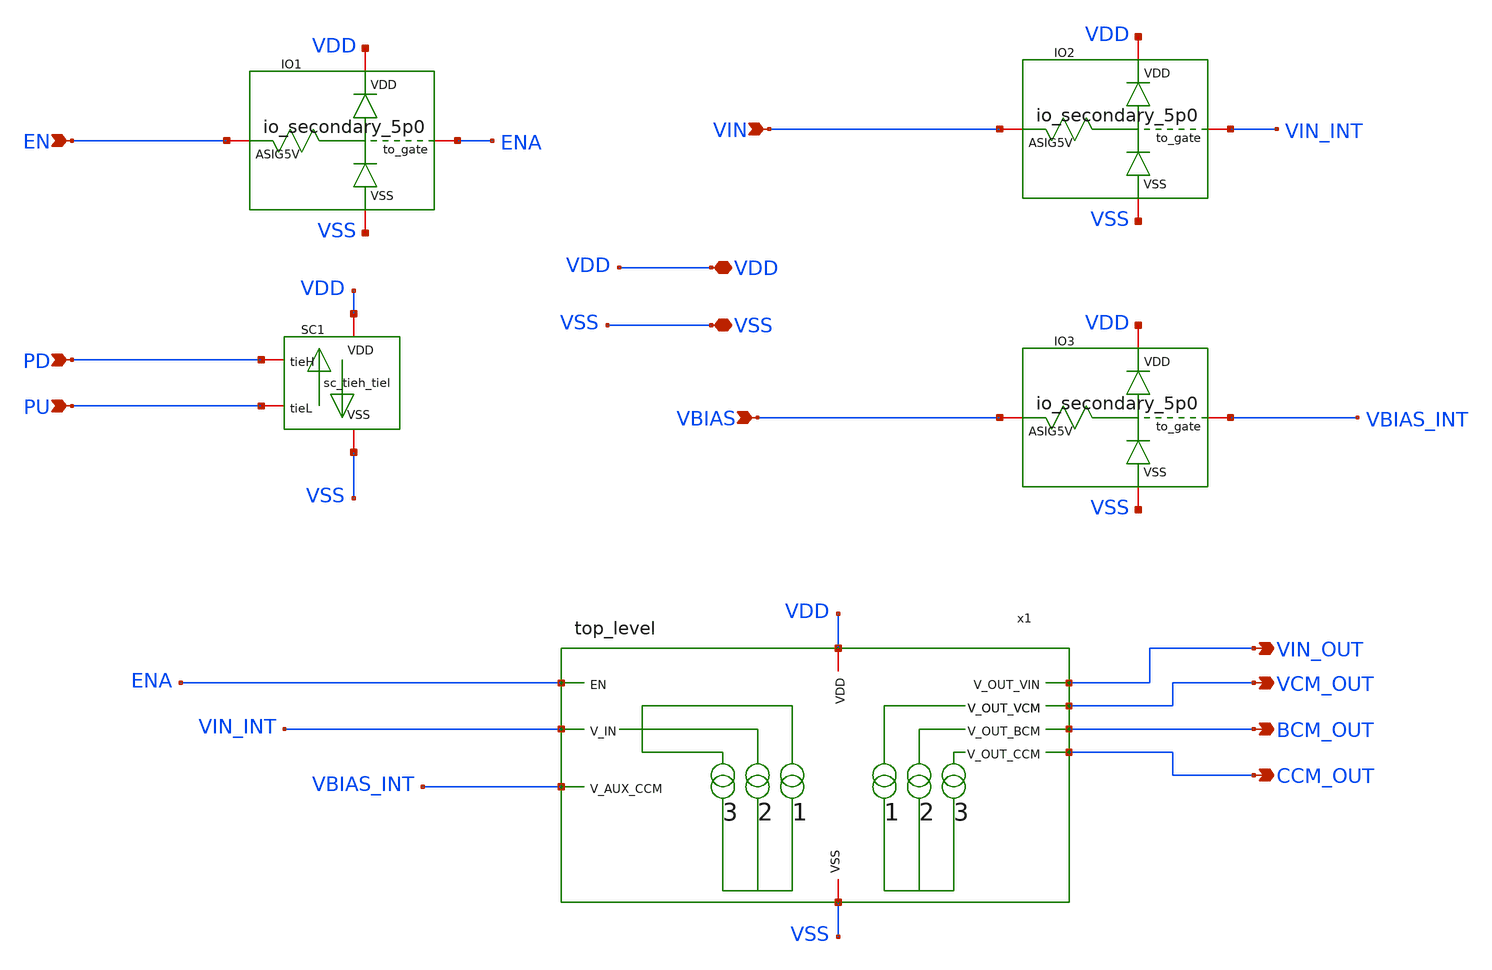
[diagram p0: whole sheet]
** sch_path: designs/libs/A3_core/A3_top/A3_top.sch
**.subckt A3_top VDD VSS VIN VBIAS VCM_OUT BCM_OUT CCM_OUT VIN_OUT PU PD EN
*.iopin VDD
*.iopin VSS
*.ipin VIN
*.ipin VBIAS
*.opin VCM_OUT
*.opin BCM_OUT
*.opin CCM_OUT
*.opin VIN_OUT
*.ipin PU
*.ipin PD
*.ipin EN
XIO1 VDD ENA EN VSS io_secondary_5p0
XIO2 VDD VIN_INT VIN VSS io_secondary_5p0
XIO3 VDD VBIAS_INT VBIAS VSS io_secondary_5p0
XSC1 PU VDD VSS PD sc_tieh_tiel
x1 VDD ENA VIN_INT VCM_OUT BCM_OUT CCM_OUT VBIAS_INT VSS VIN_OUT top_level
**.ends
.end
